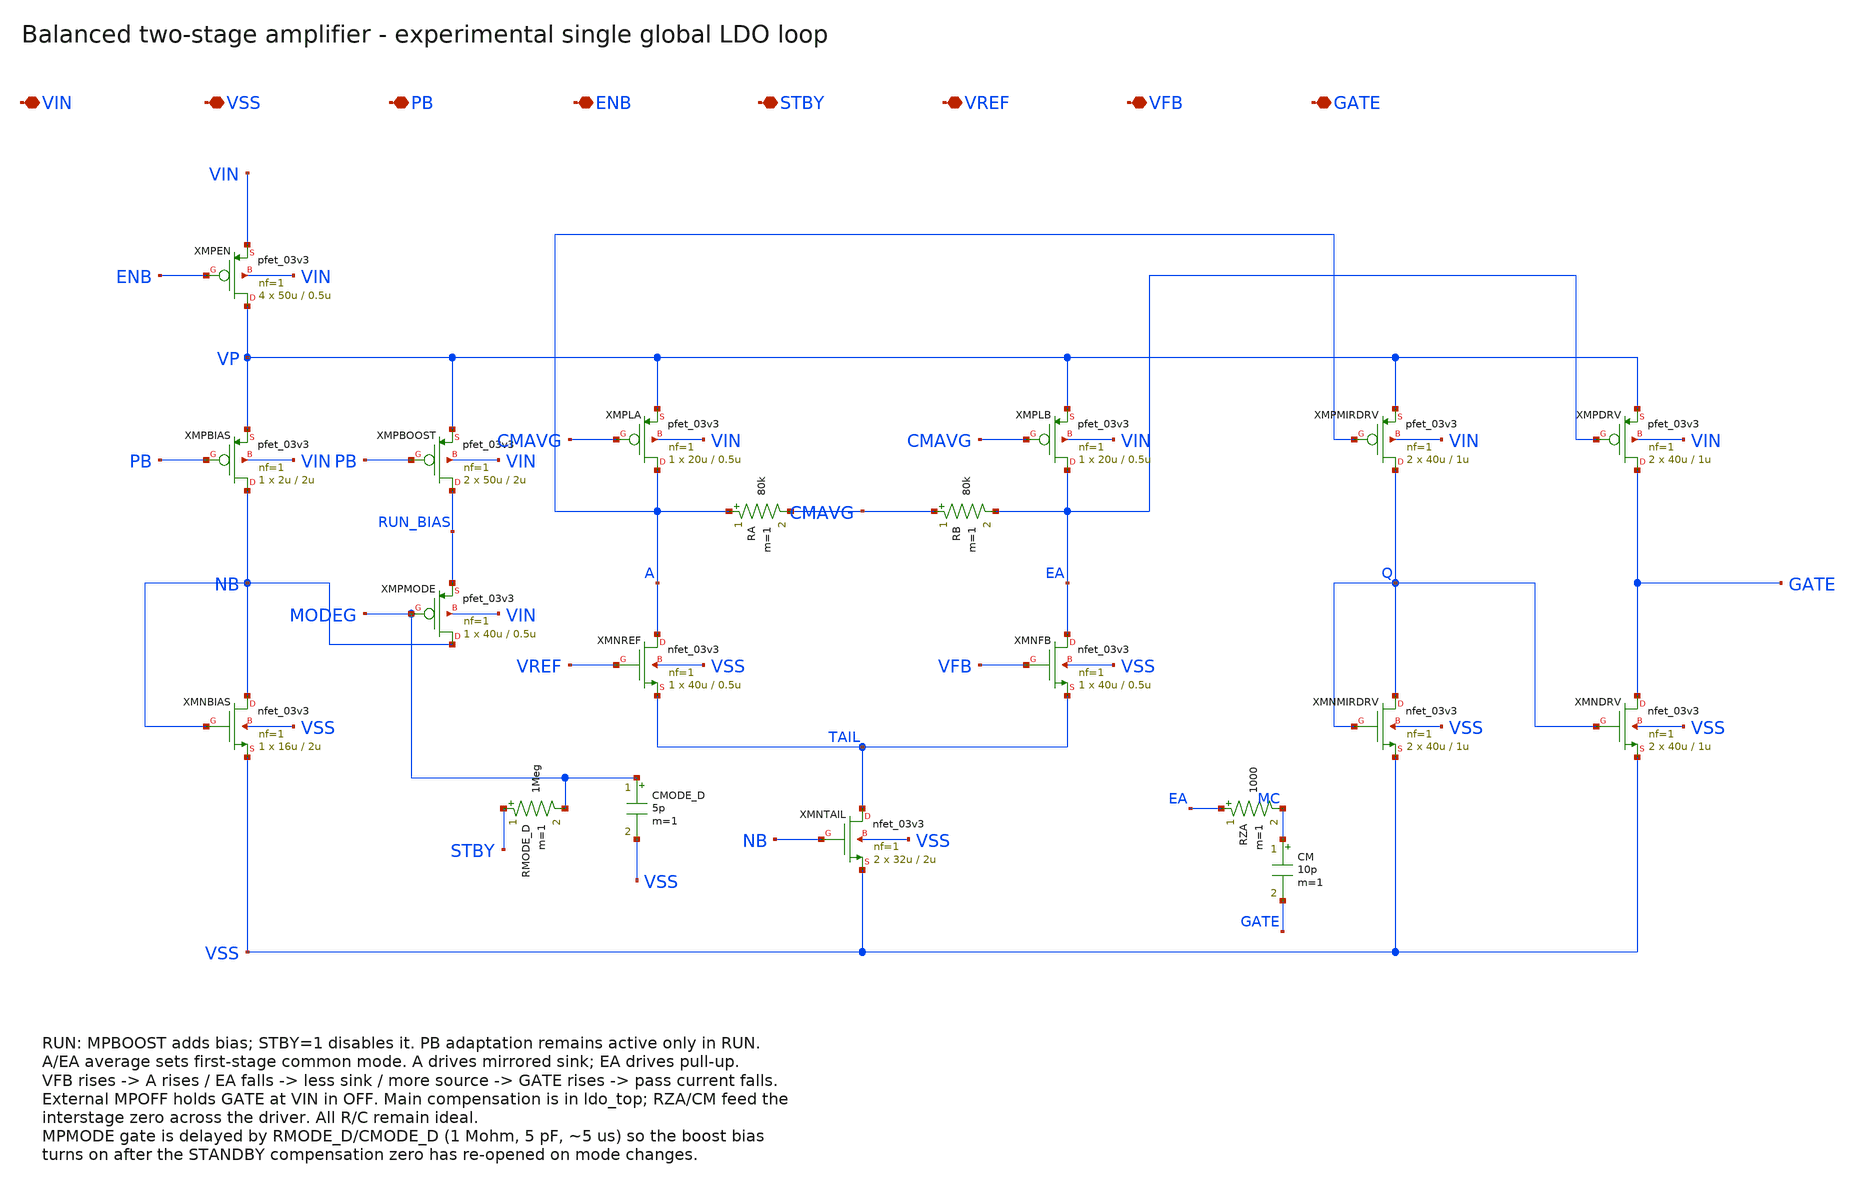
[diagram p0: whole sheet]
** sch_path: schematics/ldo_error_amp.sch
**.subckt ldo_error_amp VIN VSS PB ENB STBY VREF VFB GATE
*.iopin VIN
*.iopin VSS
*.iopin PB
*.iopin ENB
*.iopin STBY
*.iopin VREF
*.iopin VFB
*.iopin GATE
XMPEN VP ENB VIN VIN pfet_03v3 L=0.5u W=50u nf=1 ad='int((nf+1)/2)*W/nf*0.18u' as='int((nf+2)/2)*W/nf*0.18u'
+ pd='2*int((nf+1)/2)*(W/nf+0.18u)' ps='2*int((nf+2)/2)*(W/nf+0.18u)' nrd='0.18u/W' nrs='0.18u/W' sa=0
+ sb=0 sd=0 m=4 par=4
XMPBIAS NB PB VP VIN pfet_03v3 L=2u W=2u nf=1 ad='int((nf+1)/2)*W/nf*0.18u' as='int((nf+2)/2)*W/nf*0.18u'
+ pd='2*int((nf+1)/2)*(W/nf+0.18u)' ps='2*int((nf+2)/2)*(W/nf+0.18u)' nrd='0.18u/W' nrs='0.18u/W' sa=0
+ sb=0 sd=0 m=1 par=1
XMNBIAS NB NB VSS VSS nfet_03v3 L=2u W=16u nf=1 ad='int((nf+1)/2)*W/nf*0.18u' as='int((nf+2)/2)*W/nf*0.18u'
+ pd='2*int((nf+1)/2)*(W/nf+0.18u)' ps='2*int((nf+2)/2)*(W/nf+0.18u)' nrd='0.18u/W' nrs='0.18u/W' sa=0
+ sb=0 sd=0 m=1 par=1
XMPBOOST RUN_BIAS PB VP VIN pfet_03v3 L=2u W=50u nf=1 ad='int((nf+1)/2)*W/nf*0.18u' as='int((nf+2)/2)*W/nf*0.18u'
+ pd='2*int((nf+1)/2)*(W/nf+0.18u)' ps='2*int((nf+2)/2)*(W/nf+0.18u)' nrd='0.18u/W' nrs='0.18u/W' sa=0
+ sb=0 sd=0 m=2 par=2
XMPMODE NB MODEG RUN_BIAS VIN pfet_03v3 L=0.5u W=40u nf=1 ad='int((nf+1)/2)*W/nf*0.18u' as='int((nf+2)/2)*W/nf*0.18u'
+ pd='2*int((nf+1)/2)*(W/nf+0.18u)' ps='2*int((nf+2)/2)*(W/nf+0.18u)' nrd='0.18u/W' nrs='0.18u/W' sa=0
+ sb=0 sd=0 m=1 par=1
RMODE_D STBY MODEG 1Meg m=1
CMODE_D MODEG VSS 5p m=1
XMPLA A CMAVG VP VIN pfet_03v3 L=0.5u W=20u nf=1 ad='int((nf+1)/2)*W/nf*0.18u' as='int((nf+2)/2)*W/nf*0.18u'
+ pd='2*int((nf+1)/2)*(W/nf+0.18u)' ps='2*int((nf+2)/2)*(W/nf+0.18u)' nrd='0.18u/W' nrs='0.18u/W' sa=0
+ sb=0 sd=0 m=1 par=1
XMPLB EA CMAVG VP VIN pfet_03v3 L=0.5u W=20u nf=1 ad='int((nf+1)/2)*W/nf*0.18u' as='int((nf+2)/2)*W/nf*0.18u'
+ pd='2*int((nf+1)/2)*(W/nf+0.18u)' ps='2*int((nf+2)/2)*(W/nf+0.18u)' nrd='0.18u/W' nrs='0.18u/W' sa=0
+ sb=0 sd=0 m=1 par=1
RA A CMAVG 80k m=1
RB CMAVG EA 80k m=1
XMNREF A VREF TAIL VSS nfet_03v3 L=0.5u W=40u nf=1 ad='int((nf+1)/2)*W/nf*0.18u' as='int((nf+2)/2)*W/nf*0.18u'
+ pd='2*int((nf+1)/2)*(W/nf+0.18u)' ps='2*int((nf+2)/2)*(W/nf+0.18u)' nrd='0.18u/W' nrs='0.18u/W' sa=0
+ sb=0 sd=0 m=1 par=1
XMNFB EA VFB TAIL VSS nfet_03v3 L=0.5u W=40u nf=1 ad='int((nf+1)/2)*W/nf*0.18u' as='int((nf+2)/2)*W/nf*0.18u'
+ pd='2*int((nf+1)/2)*(W/nf+0.18u)' ps='2*int((nf+2)/2)*(W/nf+0.18u)' nrd='0.18u/W' nrs='0.18u/W' sa=0
+ sb=0 sd=0 m=1 par=1
XMNTAIL TAIL NB VSS VSS nfet_03v3 L=2u W=32u nf=1 ad='int((nf+1)/2)*W/nf*0.18u' as='int((nf+2)/2)*W/nf*0.18u'
+ pd='2*int((nf+1)/2)*(W/nf+0.18u)' ps='2*int((nf+2)/2)*(W/nf+0.18u)' nrd='0.18u/W' nrs='0.18u/W' sa=0
+ sb=0 sd=0 m=2 par=2
XMPMIRDRV Q A VP VIN pfet_03v3 L=1u W=40u nf=1 ad='int((nf+1)/2)*W/nf*0.18u' as='int((nf+2)/2)*W/nf*0.18u'
+ pd='2*int((nf+1)/2)*(W/nf+0.18u)' ps='2*int((nf+2)/2)*(W/nf+0.18u)' nrd='0.18u/W' nrs='0.18u/W' sa=0
+ sb=0 sd=0 m=2 par=2
XMPDRV GATE EA VP VIN pfet_03v3 L=1u W=40u nf=1 ad='int((nf+1)/2)*W/nf*0.18u' as='int((nf+2)/2)*W/nf*0.18u'
+ pd='2*int((nf+1)/2)*(W/nf+0.18u)' ps='2*int((nf+2)/2)*(W/nf+0.18u)' nrd='0.18u/W' nrs='0.18u/W' sa=0
+ sb=0 sd=0 m=2 par=2
XMNMIRDRV Q Q VSS VSS nfet_03v3 L=1u W=40u nf=1 ad='int((nf+1)/2)*W/nf*0.18u' as='int((nf+2)/2)*W/nf*0.18u'
+ pd='2*int((nf+1)/2)*(W/nf+0.18u)' ps='2*int((nf+2)/2)*(W/nf+0.18u)' nrd='0.18u/W' nrs='0.18u/W' sa=0
+ sb=0 sd=0 m=2 par=2
XMNDRV GATE Q VSS VSS nfet_03v3 L=1u W=40u nf=1 ad='int((nf+1)/2)*W/nf*0.18u' as='int((nf+2)/2)*W/nf*0.18u'
+ pd='2*int((nf+1)/2)*(W/nf+0.18u)' ps='2*int((nf+2)/2)*(W/nf+0.18u)' nrd='0.18u/W' nrs='0.18u/W' sa=0
+ sb=0 sd=0 m=2 par=2
RZA EA MC 1000 m=1
CM MC GATE 10p m=1
**.ends
.end
